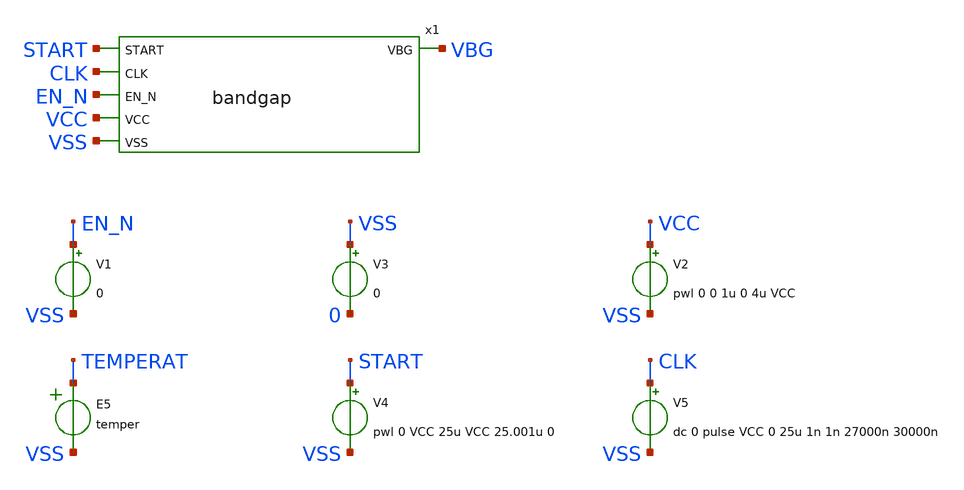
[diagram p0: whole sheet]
** sch_path: sky130_tests/tb_bandgap.sch
* Copyright 2020 Stefan Frederik Schippers
* Licensed under the Apache License, Version 2.0 (the "License");
* you may not use this file except in compliance with the License.
* You may obtain a copy of the License at
* https://www.apache.org/licenses/LICENSE-2.0
* Unless required by applicable law or agreed to in writing, software
* distributed under the License is distributed on an "AS IS" BASIS,
* WITHOUT WARRANTIES OR CONDITIONS OF ANY KIND, either express or implied.
* See the License for the specific language governing permissions and
* limitations under the License.
**.subckt tb_bandgap
x1 START CLK EN_N VBG VCC VSS bandgap
V1 EN_N VSS 0
V2 VCC VSS pwl 0 0 1u 0 4u VCC
V3 VSS 0 0
E5 TEMPERAT VSS VOL=' temper '
V4 START VSS pwl 0 VCC 25u VCC 25.001u 0
V5 CLK VSS dc 0 pulse VCC 0 25u 1n 1n 27000n 30000n
**** begin user architecture code

.option seed=3

* this experimental option enables mos model bin
* selection based on W/NF instead of W
.options wnflag=1 XMU=0.49 METHOD=GEAR ITL4=100 CHGTOL=1e-15 TRTOL=1 RELTOL=0.0001 VNTOL=0.1u
.param ABSVAR=0.03
.param VCCGAUSS=agauss(1.8, 'ABSVAR', 1)
.param VCC=VCCGAUSS
* .param VCC=1.8
** variation marameters:
.param sky130_fd_pr__nfet_01v8_lvt__vth0_slope_spectre='agauss(0, ABSVAR, 3)/sky130_fd_pr__nfet_01v8_lvt__vth0_slope'
.param sky130_fd_pr__pfet_01v8_lvt__vth0_slope_spectre='agauss(0, ABSVAR, 3)/sky130_fd_pr__pfet_01v8_lvt__vth0_slope'
.param sky130_fd_pr__nfet_01v8__vth0_slope_spectre='agauss(0, ABSVAR, 3)/sky130_fd_pr__nfet_01v8__vth0_slope'
.param sky130_fd_pr__pfet_01v8__vth0_slope_spectre='agauss(0, ABSVAR, 3)/sky130_fd_pr__pfet_01v8__vth0_slope'

.param sky130_fd_pr__pfet_01v8__toxe_slope_spectre='agauss(0, ABSVAR, 3)/sky130_fd_pr__pfet_01v8__toxe_slope'
.param sky130_fd_pr__nfet_01v8__toxe_slope_spectre='agauss(0, ABSVAR, 3)/sky130_fd_pr__nfet_01v8__toxe_slope'
.param sky130_fd_pr__pfet_01v8_lvt__toxe_slope_spectre='agauss(0, ABSVAR, 3)/sky130_fd_pr__pfet_01v8_lvt__toxe_slope'
.param sky130_fd_pr__nfet_01v8_lvt__toxe_slope_spectre='agauss(0, ABSVAR, 3)/sky130_fd_pr__nfet_01v8_lvt__toxe_slope'

.param sky130_fd_pr__res_xhigh_po__var_mult='agauss(0, ABSVAR, 3)'

* .options savecurrents
.control
  let run=1
  dowhile run <= 4
    if run > 1
      reset
      set appendwrite
    end
    * save vbg x1.plus x1.minus i(v2) vcc
    save all
    if run % 3 = 0
      set temp=-40
    end
    if run % 3 = 1
      set temp=27
    end
    if run % 3 = 2
      set temp=125
    end
    tran 0.05u 150u
    write tb_bandgap.raw
    let run = run + 1
  end
  set nolegend
  plot all.vbg
.endc



.include $::SKYWATER_MODELS/cells/nfet_01v8/sky130_fd_pr__nfet_01v8__tt.corner.spice
.include $::SKYWATER_MODELS/cells/nfet_01v8_lvt/sky130_fd_pr__nfet_01v8_lvt__tt.corner.spice
.include $::SKYWATER_MODELS/cells/pfet_01v8/sky130_fd_pr__pfet_01v8__tt.corner.spice
.include $::SKYWATER_MODELS/cells/nfet_03v3_nvt/sky130_fd_pr__nfet_03v3_nvt__tt.corner.spice
.include $::SKYWATER_MODELS/cells/nfet_05v0_nvt/sky130_fd_pr__nfet_05v0_nvt__tt.corner.spice
.include $::SKYWATER_MODELS/cells/esd_nfet_01v8/sky130_fd_pr__esd_nfet_01v8__tt.corner.spice
.include $::SKYWATER_MODELS/cells/pfet_01v8_lvt/sky130_fd_pr__pfet_01v8_lvt__tt.corner.spice
.include $::SKYWATER_MODELS/cells/pfet_01v8_hvt/sky130_fd_pr__pfet_01v8_hvt__tt.corner.spice
.include $::SKYWATER_MODELS/cells/esd_pfet_g5v0d10v5/sky130_fd_pr__esd_pfet_g5v0d10v5__tt.corner.spice
.include $::SKYWATER_MODELS/cells/pfet_g5v0d10v5/sky130_fd_pr__pfet_g5v0d10v5__tt.corner.spice
.include $::SKYWATER_MODELS/cells/pfet_g5v0d16v0/sky130_fd_pr__pfet_g5v0d16v0__tt.corner.spice
.include $::SKYWATER_MODELS/cells/nfet_g5v0d10v5/sky130_fd_pr__nfet_g5v0d10v5__tt.corner.spice
.include $::SKYWATER_MODELS/cells/nfet_g5v0d16v0/sky130_fd_pr__nfet_g5v0d16v0__tt_discrete.corner.spice
.include $::SKYWATER_MODELS/cells/esd_nfet_g5v0d10v5/sky130_fd_pr__esd_nfet_g5v0d10v5__tt.corner.spice
.include $::SKYWATER_MODELS/models/corners/tt/nonfet.spice
* Mismatch parameters
.include $::SKYWATER_MODELS/cells/nfet_01v8/sky130_fd_pr__nfet_01v8__mismatch.corner.spice
.include $::SKYWATER_MODELS/cells/pfet_01v8/sky130_fd_pr__pfet_01v8__mismatch.corner.spice
.include $::SKYWATER_MODELS/cells/nfet_01v8_lvt/sky130_fd_pr__nfet_01v8_lvt__mismatch.corner.spice
.include $::SKYWATER_MODELS/cells/pfet_01v8_lvt/sky130_fd_pr__pfet_01v8_lvt__mismatch.corner.spice
.include $::SKYWATER_MODELS/cells/pfet_01v8_hvt/sky130_fd_pr__pfet_01v8_hvt__mismatch.corner.spice
.include $::SKYWATER_MODELS/cells/nfet_g5v0d10v5/sky130_fd_pr__nfet_g5v0d10v5__mismatch.corner.spice
.include $::SKYWATER_MODELS/cells/pfet_g5v0d10v5/sky130_fd_pr__pfet_g5v0d10v5__mismatch.corner.spice
.include $::SKYWATER_MODELS/cells/nfet_05v0_nvt/sky130_fd_pr__nfet_05v0_nvt__mismatch.corner.spice
.include $::SKYWATER_MODELS/cells/nfet_03v3_nvt/sky130_fd_pr__nfet_03v3_nvt__mismatch.corner.spice
* Resistor$::SKYWATER_MODELS/Capacitor
.include $::SKYWATER_MODELS/models/r+c/res_typical__cap_typical.spice
.include $::SKYWATER_MODELS/models/r+c/res_typical__cap_typical__lin.spice
* Special cells
.include $::SKYWATER_MODELS/models/corners/tt/specialized_cells.spice
* All models
.include $::SKYWATER_MODELS/models/all.spice
* Corner
.include $::SKYWATER_MODELS/models/corners/tt/rf.spice

**** end user architecture code
**.ends
.end
